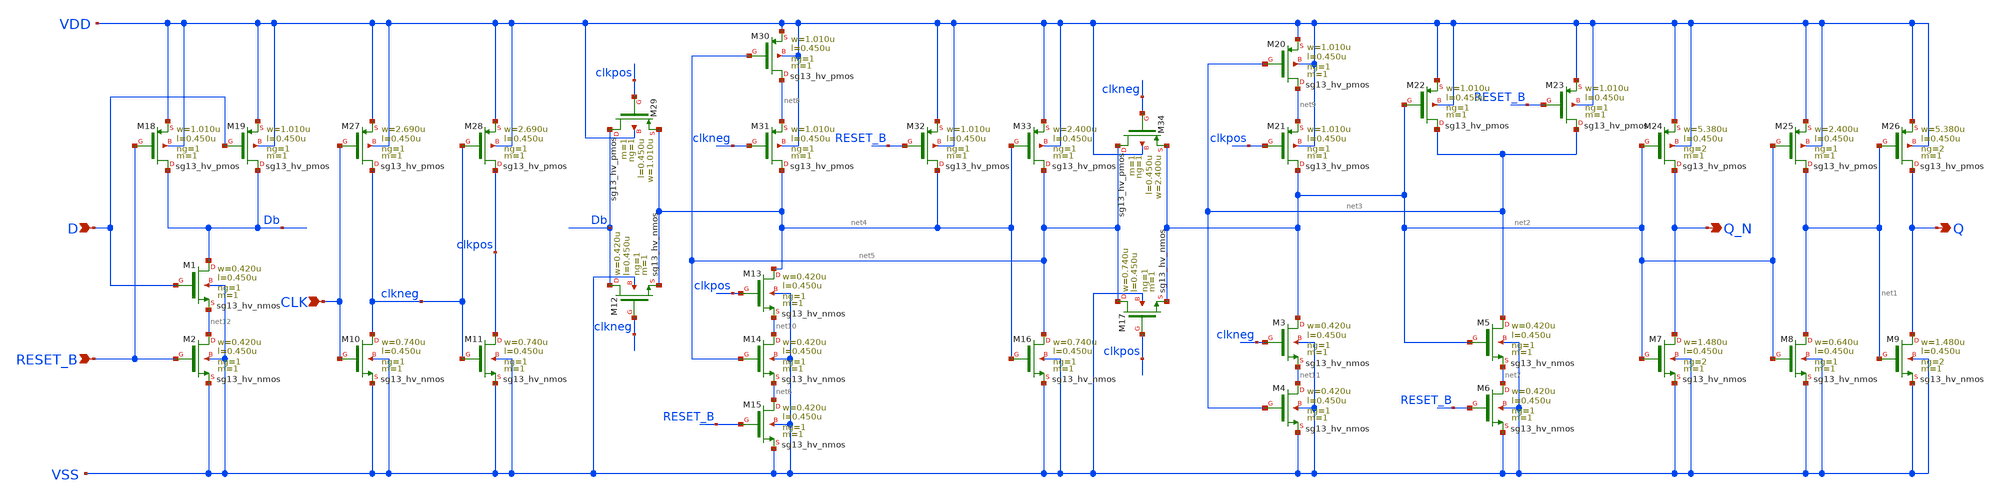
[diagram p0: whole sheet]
** sch_path: ihp-sg13g2/libs.ref/sg13g2_stdcell_hv/sch/xschem/sg13g2_hv_dfrbp_2.sch
* Copyright 2023 IHP PDK Authors
* Licensed under the Apache License, Version 2.0 (the "License");
* you may not use this file except in compliance with the License.
* You may obtain a copy of the License at
* https://www.apache.org/licenses/LICENSE-2.0
* Unless required by applicable law or agreed to in writing, software
* distributed under the License is distributed on an "AS IS" BASIS,
* WITHOUT WARRANTIES OR CONDITIONS OF ANY KIND, either express or implied.
* See the License for the specific language governing permissions and
* limitations under the License.
**.subckt sg13g2_hv_dfrbp_2 D RESET_B CLK Q Q_N
*.ipin D
*.ipin RESET_B
*.ipin CLK
*.opin Q
*.opin Q_N
XM1 Db D net12 VSS sg13_hv_nmos w=0.420u l=0.450u ng=1 m=1 mm_ok=1
XM2 net12 RESET_B VSS VSS sg13_hv_nmos w=0.420u l=0.450u ng=1 m=1 mm_ok=1
XM3 net2 clkneg net11 VSS sg13_hv_nmos w=0.420u l=0.450u ng=1 m=1 mm_ok=1
XM4 net11 net3 VSS VSS sg13_hv_nmos w=0.420u l=0.450u ng=1 m=1 mm_ok=1
XM5 net3 net2 net7 VSS sg13_hv_nmos w=0.420u l=0.450u ng=1 m=1 mm_ok=1
XM6 net7 RESET_B VSS VSS sg13_hv_nmos w=0.420u l=0.450u ng=1 m=1 mm_ok=1
XM7 Q_N net2 VSS VSS sg13_hv_nmos w=1.480u l=0.450u ng=2 m=1 mm_ok=1
XM8 net1 net2 VSS VSS sg13_hv_nmos w=0.640u l=0.450u ng=1 m=1 mm_ok=1
XM9 Q net1 VSS VSS sg13_hv_nmos w=1.480u l=0.450u ng=2 m=1 mm_ok=1
XM10 clkneg CLK VSS VSS sg13_hv_nmos w=0.740u l=0.450u ng=1 m=1 mm_ok=1
XM11 clkpos clkneg VSS VSS sg13_hv_nmos w=0.740u l=0.450u ng=1 m=1 mm_ok=1
XM12 Db clkneg net4 VSS sg13_hv_nmos w=0.420u l=0.450u ng=1 m=1 mm_ok=1
XM13 net4 clkpos net10 VSS sg13_hv_nmos w=0.420u l=0.450u ng=1 m=1 mm_ok=1
XM14 net10 net5 net6 VSS sg13_hv_nmos w=0.420u l=0.450u ng=1 m=1 mm_ok=1
XM15 net6 RESET_B VSS VSS sg13_hv_nmos w=0.420u l=0.450u ng=1 m=1 mm_ok=1
XM16 net5 net4 VSS VSS sg13_hv_nmos w=0.740u l=0.450u ng=1 m=1 mm_ok=1
XM17 net5 clkpos net2 VSS sg13_hv_nmos w=0.740u l=0.450u ng=1 m=1 mm_ok=1
XM18 Db RESET_B VDD VDD sg13_hv_pmos w=1.010u l=0.450u ng=1 m=1 mm_ok=1
XM19 Db D VDD VDD sg13_hv_pmos w=1.010u l=0.450u ng=1 m=1 mm_ok=1
XM20 net9 net3 VDD VDD sg13_hv_pmos w=1.010u l=0.450u ng=1 m=1 mm_ok=1
XM21 net2 clkpos net9 VDD sg13_hv_pmos w=1.010u l=0.450u ng=1 m=1 mm_ok=1
XM22 net3 net2 VDD VDD sg13_hv_pmos w=1.010u l=0.450u ng=1 m=1 mm_ok=1
XM23 net3 RESET_B VDD VDD sg13_hv_pmos w=1.010u l=0.450u ng=1 m=1 mm_ok=1
XM24 Q_N net2 VDD VDD sg13_hv_pmos w=5.380u l=0.450u ng=2 m=1 mm_ok=1
XM25 net1 net2 VDD VDD sg13_hv_pmos w=2.400u l=0.450u ng=1 m=1 mm_ok=1
XM26 Q net1 VDD VDD sg13_hv_pmos w=5.380u l=0.450u ng=2 m=1 mm_ok=1
XM27 clkneg CLK VDD VDD sg13_hv_pmos w=2.690u l=0.450u ng=1 m=1 mm_ok=1
XM28 clkpos clkneg VDD VDD sg13_hv_pmos w=2.690u l=0.450u ng=1 m=1 mm_ok=1
XM29 Db clkpos net4 VDD sg13_hv_pmos w=1.010u l=0.450u ng=1 m=1 mm_ok=1
XM30 net8 net5 VDD VDD sg13_hv_pmos w=1.010u l=0.450u ng=1 m=1 mm_ok=1
XM31 net4 clkneg net8 VDD sg13_hv_pmos w=1.010u l=0.450u ng=1 m=1 mm_ok=1
XM32 net4 RESET_B VDD VDD sg13_hv_pmos w=1.010u l=0.450u ng=1 m=1 mm_ok=1
XM33 net5 net4 VDD VDD sg13_hv_pmos w=2.400u l=0.450u ng=1 m=1 mm_ok=1
XM34 net5 clkneg net2 VDD sg13_hv_pmos w=2.400u l=0.450u ng=1 m=1 mm_ok=1
**.ends
.end
